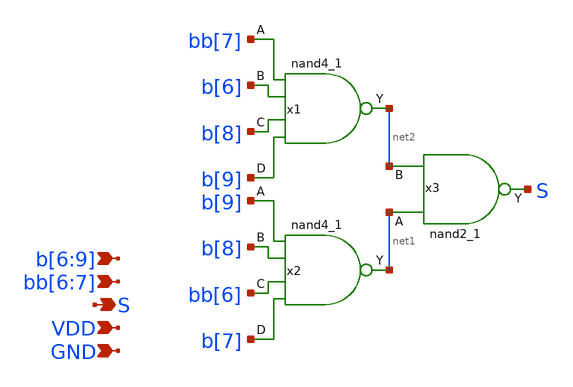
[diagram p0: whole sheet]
** sch_path: xschem/seg_selector_3_logic.sch
**.subckt seg_selector_3_logic S GND VDD b[6],b[7],b[8],b[9] bb[6],bb[7]
*.opin S
*.ipin GND
*.ipin VDD
*.ipin b[6],b[7],b[8],b[9]
*.ipin bb[6],bb[7]
x2 b[9] b[8] bb[6] b[7] GND GND VDD VDD net1 sky130_fd_sc_hd__nand4_1
x1 bb[7] b[6] b[8] b[9] GND GND VDD VDD net2 sky130_fd_sc_hd__nand4_1
x3 net1 net2 GND GND VDD VDD S sky130_fd_sc_hd__nand2_1
**.ends
.end
